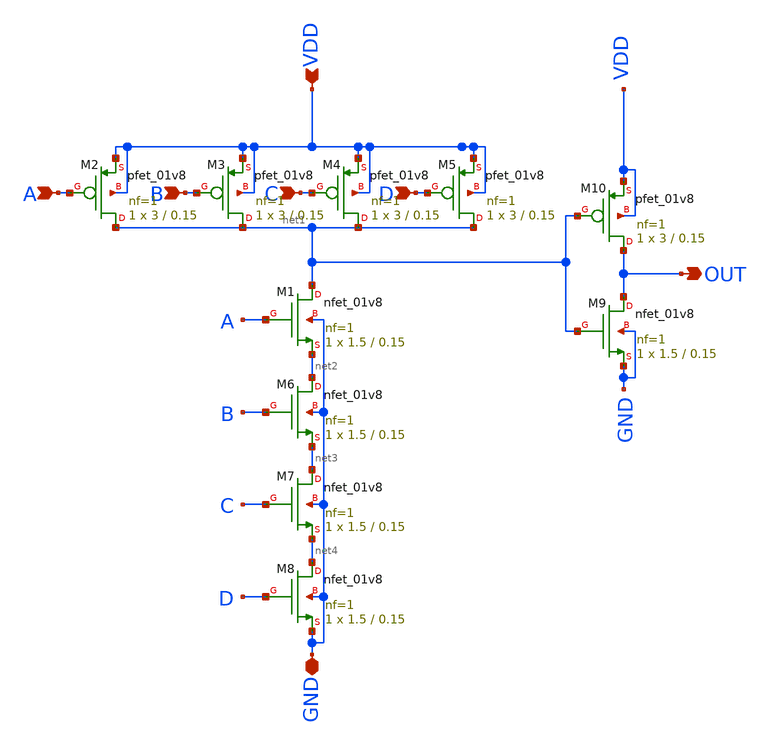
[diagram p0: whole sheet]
** sch_path: skywater_stuff/CMOS_4in_AND.sch
**.subckt CMOS_4in_AND A B C D OUT GND VDD
*.ipin A
*.ipin B
*.ipin C
*.ipin D
*.opin OUT
*.iopin GND
*.ipin VDD
XM3 net1 B VDD VDD sky130_fd_pr__pfet_01v8 L=0.15 W=3 nf=1 ad='int((nf+1)/2) * W/nf * 0.29' as='int((nf+2)/2) * W/nf * 0.29'
+ pd='2*int((nf+1)/2) * (W/nf + 0.29)' ps='2*int((nf+2)/2) * (W/nf + 0.29)' nrd='0.29 / W' nrs='0.29 / W'
+ sa=0 sb=0 sd=0 mult=1 m=1
XM4 net1 C VDD VDD sky130_fd_pr__pfet_01v8 L=0.15 W=3 nf=1 ad='int((nf+1)/2) * W/nf * 0.29' as='int((nf+2)/2) * W/nf * 0.29'
+ pd='2*int((nf+1)/2) * (W/nf + 0.29)' ps='2*int((nf+2)/2) * (W/nf + 0.29)' nrd='0.29 / W' nrs='0.29 / W'
+ sa=0 sb=0 sd=0 mult=1 m=1
XM6 net2 B net3 GND sky130_fd_pr__nfet_01v8 L=0.15 W=1.5 nf=1 ad='int((nf+1)/2) * W/nf * 0.29' as='int((nf+2)/2) * W/nf * 0.29'
+ pd='2*int((nf+1)/2) * (W/nf + 0.29)' ps='2*int((nf+2)/2) * (W/nf + 0.29)' nrd='0.29 / W' nrs='0.29 / W'
+ sa=0 sb=0 sd=0 mult=1 m=1
XM7 net3 C net4 GND sky130_fd_pr__nfet_01v8 L=0.15 W=1.5 nf=1 ad='int((nf+1)/2) * W/nf * 0.29' as='int((nf+2)/2) * W/nf * 0.29'
+ pd='2*int((nf+1)/2) * (W/nf + 0.29)' ps='2*int((nf+2)/2) * (W/nf + 0.29)' nrd='0.29 / W' nrs='0.29 / W'
+ sa=0 sb=0 sd=0 mult=1 m=1
XM8 net4 D GND GND sky130_fd_pr__nfet_01v8 L=0.15 W=1.5 nf=1 ad='int((nf+1)/2) * W/nf * 0.29' as='int((nf+2)/2) * W/nf * 0.29'
+ pd='2*int((nf+1)/2) * (W/nf + 0.29)' ps='2*int((nf+2)/2) * (W/nf + 0.29)' nrd='0.29 / W' nrs='0.29 / W'
+ sa=0 sb=0 sd=0 mult=1 m=1
XM9 OUT net1 GND GND sky130_fd_pr__nfet_01v8 L=0.15 W=1.5 nf=1 ad='int((nf+1)/2) * W/nf * 0.29' as='int((nf+2)/2) * W/nf * 0.29'
+ pd='2*int((nf+1)/2) * (W/nf + 0.29)' ps='2*int((nf+2)/2) * (W/nf + 0.29)' nrd='0.29 / W' nrs='0.29 / W'
+ sa=0 sb=0 sd=0 mult=1 m=1
XM10 OUT net1 VDD VDD sky130_fd_pr__pfet_01v8 L=0.15 W=3 nf=1 ad='int((nf+1)/2) * W/nf * 0.29' as='int((nf+2)/2) * W/nf * 0.29'
+ pd='2*int((nf+1)/2) * (W/nf + 0.29)' ps='2*int((nf+2)/2) * (W/nf + 0.29)' nrd='0.29 / W' nrs='0.29 / W'
+ sa=0 sb=0 sd=0 mult=1 m=1
XM1 net1 A net2 GND sky130_fd_pr__nfet_01v8 L=0.15 W=1.5 nf=1 ad='int((nf+1)/2) * W/nf * 0.29' as='int((nf+2)/2) * W/nf * 0.29'
+ pd='2*int((nf+1)/2) * (W/nf + 0.29)' ps='2*int((nf+2)/2) * (W/nf + 0.29)' nrd='0.29 / W' nrs='0.29 / W'
+ sa=0 sb=0 sd=0 mult=1 m=1
XM2 net1 A VDD VDD sky130_fd_pr__pfet_01v8 L=0.15 W=3 nf=1 ad='int((nf+1)/2) * W/nf * 0.29' as='int((nf+2)/2) * W/nf * 0.29'
+ pd='2*int((nf+1)/2) * (W/nf + 0.29)' ps='2*int((nf+2)/2) * (W/nf + 0.29)' nrd='0.29 / W' nrs='0.29 / W'
+ sa=0 sb=0 sd=0 mult=1 m=1
XM5 net1 D VDD VDD sky130_fd_pr__pfet_01v8 L=0.15 W=3 nf=1 ad='int((nf+1)/2) * W/nf * 0.29' as='int((nf+2)/2) * W/nf * 0.29'
+ pd='2*int((nf+1)/2) * (W/nf + 0.29)' ps='2*int((nf+2)/2) * (W/nf + 0.29)' nrd='0.29 / W' nrs='0.29 / W'
+ sa=0 sb=0 sd=0 mult=1 m=1
**.ends
.end
